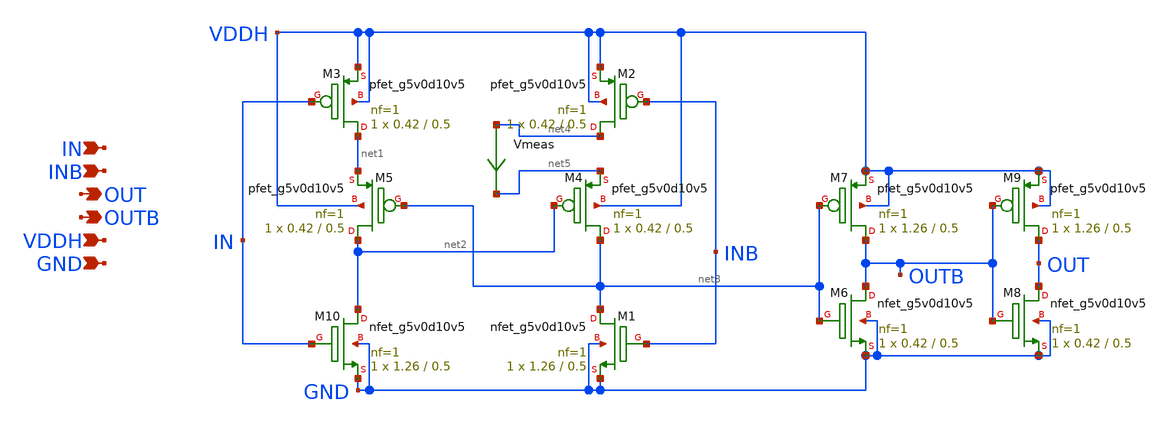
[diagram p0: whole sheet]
** sch_path: xschem/lvsf.sch
**.subckt lvsf IN INB OUT OUTB VDDH GND
*.ipin IN
*.ipin INB
*.opin OUT
*.opin OUTB
*.ipin VDDH
*.ipin GND
XM2 net4 INB VDDH VDDH sky130_fd_pr__pfet_g5v0d10v5 L=0.5 W=0.42 nf=1 ad='int((nf+1)/2) * W/nf * 0.29'
+ as='int((nf+2)/2) * W/nf * 0.29' pd='2*int((nf+1)/2) * (W/nf + 0.29)' ps='2*int((nf+2)/2) * (W/nf + 0.29)'
+ nrd='0.29 / W' nrs='0.29 / W' sa=0 sb=0 sd=0 mult=1 m=1
XM3 net1 IN VDDH VDDH sky130_fd_pr__pfet_g5v0d10v5 L=0.5 W=0.42 nf=1 ad='int((nf+1)/2) * W/nf * 0.29'
+ as='int((nf+2)/2) * W/nf * 0.29' pd='2*int((nf+1)/2) * (W/nf + 0.29)' ps='2*int((nf+2)/2) * (W/nf + 0.29)'
+ nrd='0.29 / W' nrs='0.29 / W' sa=0 sb=0 sd=0 mult=1 m=1
XM4 net3 net2 net5 VDDH sky130_fd_pr__pfet_g5v0d10v5 L=0.5 W=0.42 nf=1 ad='int((nf+1)/2) * W/nf * 0.29'
+ as='int((nf+2)/2) * W/nf * 0.29' pd='2*int((nf+1)/2) * (W/nf + 0.29)' ps='2*int((nf+2)/2) * (W/nf + 0.29)'
+ nrd='0.29 / W' nrs='0.29 / W' sa=0 sb=0 sd=0 mult=1 m=1
XM5 net2 net3 net1 VDDH sky130_fd_pr__pfet_g5v0d10v5 L=0.5 W=0.42 nf=1 ad='int((nf+1)/2) * W/nf * 0.29'
+ as='int((nf+2)/2) * W/nf * 0.29' pd='2*int((nf+1)/2) * (W/nf + 0.29)' ps='2*int((nf+2)/2) * (W/nf + 0.29)'
+ nrd='0.29 / W' nrs='0.29 / W' sa=0 sb=0 sd=0 mult=1 m=1
XM7 OUTB net3 VDDH VDDH sky130_fd_pr__pfet_g5v0d10v5 L=0.5 W=1.26 nf=1 ad='int((nf+1)/2) * W/nf * 0.29'
+ as='int((nf+2)/2) * W/nf * 0.29' pd='2*int((nf+1)/2) * (W/nf + 0.29)' ps='2*int((nf+2)/2) * (W/nf + 0.29)'
+ nrd='0.29 / W' nrs='0.29 / W' sa=0 sb=0 sd=0 mult=1 m=1
XM9 OUT OUTB VDDH VDDH sky130_fd_pr__pfet_g5v0d10v5 L=0.5 W=1.26 nf=1 ad='int((nf+1)/2) * W/nf * 0.29'
+ as='int((nf+2)/2) * W/nf * 0.29' pd='2*int((nf+1)/2) * (W/nf + 0.29)' ps='2*int((nf+2)/2) * (W/nf + 0.29)'
+ nrd='0.29 / W' nrs='0.29 / W' sa=0 sb=0 sd=0 mult=1 m=1
XM10 net2 IN GND GND sky130_fd_pr__nfet_g5v0d10v5 L=0.5 W=1.26 nf=1 ad='int((nf+1)/2) * W/nf * 0.29'
+ as='int((nf+2)/2) * W/nf * 0.29' pd='2*int((nf+1)/2) * (W/nf + 0.29)' ps='2*int((nf+2)/2) * (W/nf + 0.29)'
+ nrd='0.29 / W' nrs='0.29 / W' sa=0 sb=0 sd=0 mult=1 m=1
XM1 net3 INB GND GND sky130_fd_pr__nfet_g5v0d10v5 L=0.5 W=1.26 nf=1 ad='int((nf+1)/2) * W/nf * 0.29'
+ as='int((nf+2)/2) * W/nf * 0.29' pd='2*int((nf+1)/2) * (W/nf + 0.29)' ps='2*int((nf+2)/2) * (W/nf + 0.29)'
+ nrd='0.29 / W' nrs='0.29 / W' sa=0 sb=0 sd=0 mult=1 m=1
XM6 OUTB net3 GND GND sky130_fd_pr__nfet_g5v0d10v5 L=0.5 W=0.42 nf=1 ad='int((nf+1)/2) * W/nf * 0.29'
+ as='int((nf+2)/2) * W/nf * 0.29' pd='2*int((nf+1)/2) * (W/nf + 0.29)' ps='2*int((nf+2)/2) * (W/nf + 0.29)'
+ nrd='0.29 / W' nrs='0.29 / W' sa=0 sb=0 sd=0 mult=1 m=1
XM8 OUT OUTB GND GND sky130_fd_pr__nfet_g5v0d10v5 L=0.5 W=0.42 nf=1 ad='int((nf+1)/2) * W/nf * 0.29'
+ as='int((nf+2)/2) * W/nf * 0.29' pd='2*int((nf+1)/2) * (W/nf + 0.29)' ps='2*int((nf+2)/2) * (W/nf + 0.29)'
+ nrd='0.29 / W' nrs='0.29 / W' sa=0 sb=0 sd=0 mult=1 m=1
Vmeas net4 net5 0
.save i(vmeas)
**.ends
.end
